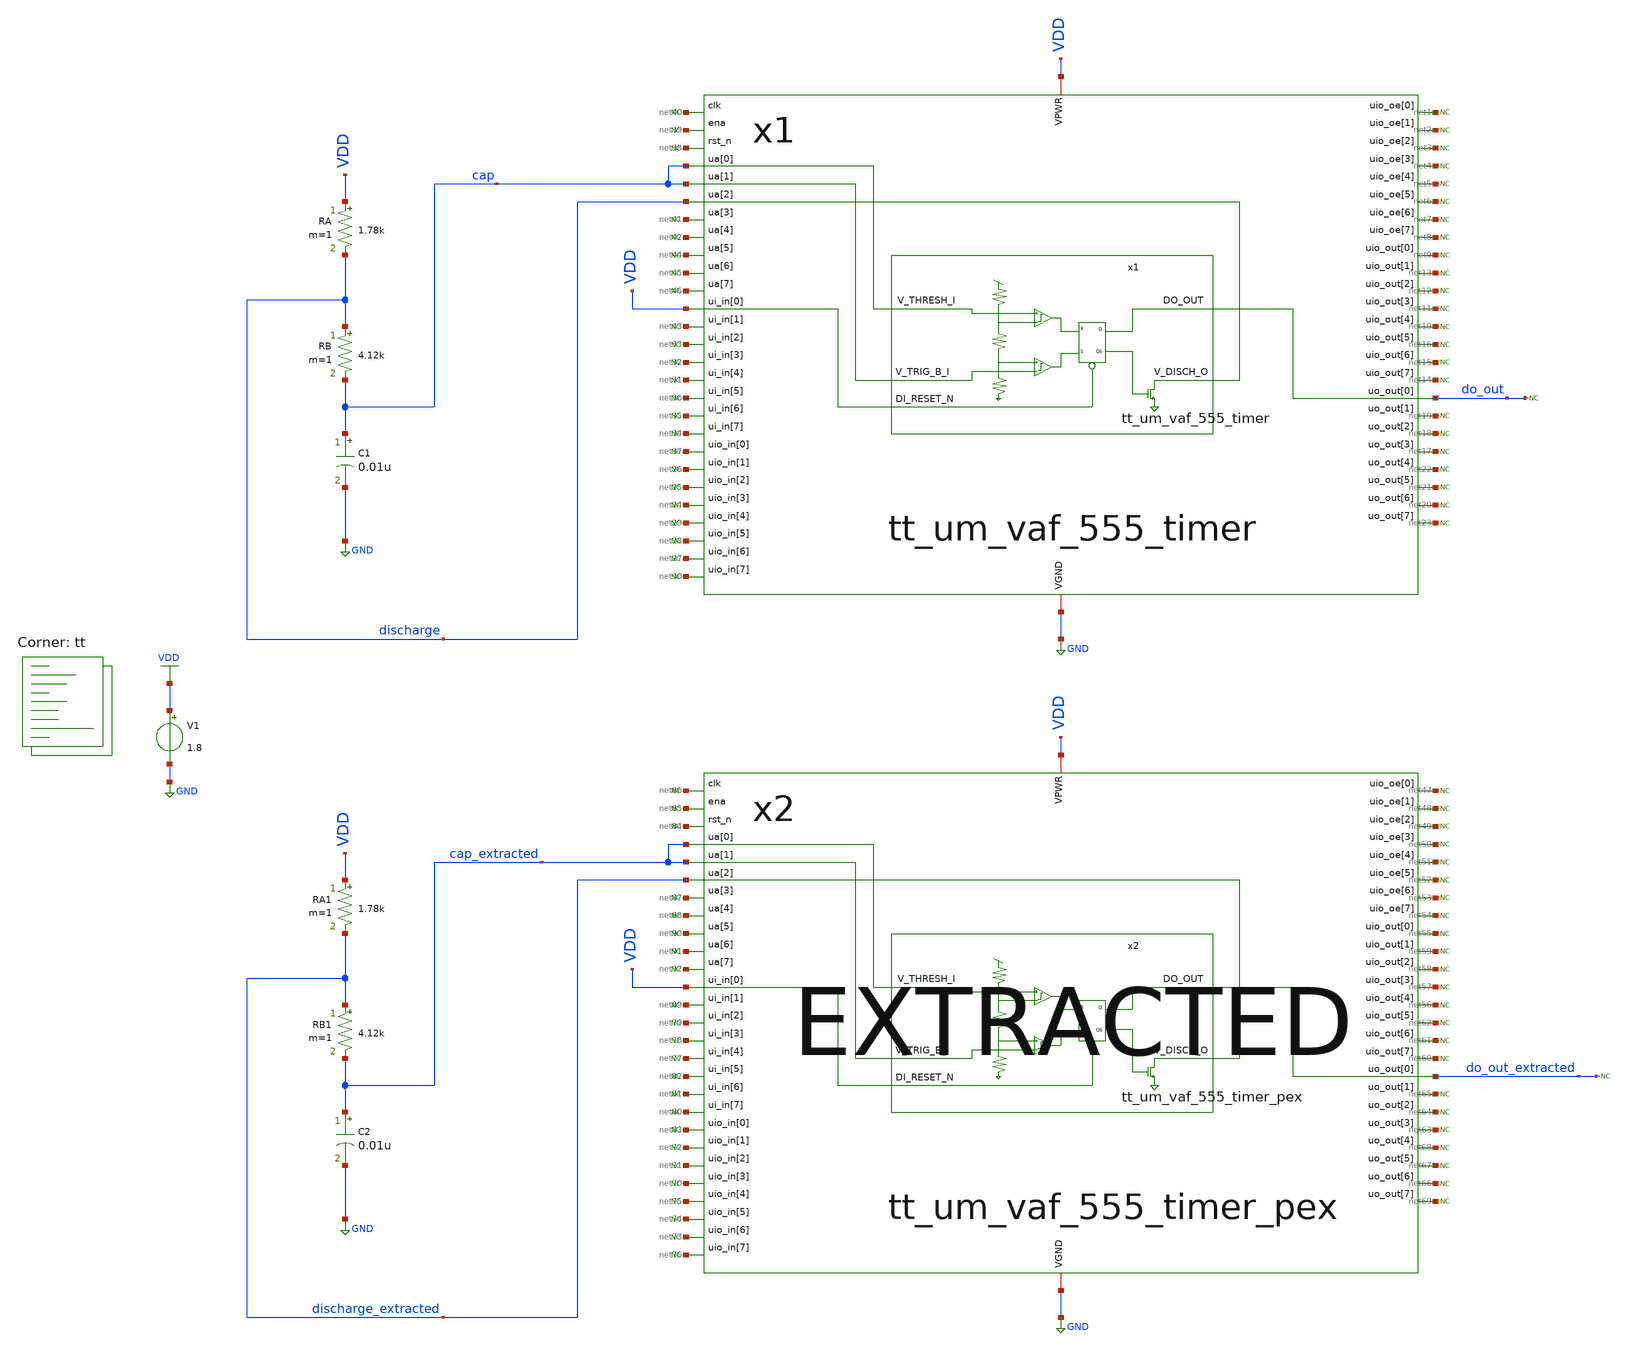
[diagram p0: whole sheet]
** sch_path: xsch/tb/tt_um_vaf_555_timer/tb_tt_um_vaf_555_timer_astable.sch
**.subckt tb_tt_um_vaf_555_timer_astable
V1 VDD GND 1.8
.save i(v1)
RA VDD discharge 1.78k m=1
RB discharge cap 4.12k m=1
C1 cap GND 0.01u m=1
* noconn do_out
* noconn #net1
* noconn #net2
* noconn #net3
* noconn #net4
* noconn #net5
* noconn #net6
* noconn #net7
* noconn #net8
* noconn #net9
* noconn #net10
* noconn #net11
* noconn #net12
* noconn #net13
* noconn #net14
* noconn #net15
* noconn #net16
* noconn #net17
* noconn #net18
* noconn #net19
* noconn #net20
* noconn #net21
* noconn #net22
* noconn #net23
* noconn #net24
* noconn #net25
* noconn #net26
* noconn #net27
* noconn #net28
* noconn #net29
* noconn #net30
* noconn #net31
* noconn #net32
* noconn #net33
* noconn #net34
* noconn #net35
* noconn #net36
* noconn #net37
* noconn #net38
* noconn #net39
* noconn #net40
* noconn #net41
* noconn #net42
* noconn #net43
x1 net40 net39 net38 cap cap discharge net41 net42 net44 net45 net46 VDD net43 net33 net32 net31
+ net36 net35 net34 net37 net26 net25 net24 net29 net28 net27 net30 net1 net2 net3 net4 net5 net6 net7 net8
+ net9 net13 net12 net11 net10 net16 net15 net14 do_out net19 net18 net17 net22 net21 net20 net23 VDD GND
+ tt_um_vaf_555_timer
* noconn #net44
* noconn #net45
* noconn #net46
RA1 VDD discharge_extracted 1.78k m=1
RB1 discharge_extracted cap_extracted 4.12k m=1
C2 cap_extracted GND 0.01u m=1
* noconn do_out_extracted
* noconn #net47
* noconn #net48
* noconn #net49
* noconn #net50
* noconn #net51
* noconn #net52
* noconn #net53
* noconn #net54
* noconn #net55
* noconn #net56
* noconn #net57
* noconn #net58
* noconn #net59
* noconn #net60
* noconn #net61
* noconn #net62
* noconn #net63
* noconn #net64
* noconn #net65
* noconn #net66
* noconn #net67
* noconn #net68
* noconn #net69
* noconn #net70
* noconn #net71
* noconn #net72
* noconn #net73
* noconn #net74
* noconn #net75
* noconn #net76
* noconn #net77
* noconn #net78
* noconn #net79
* noconn #net80
* noconn #net81
* noconn #net82
* noconn #net83
* noconn #net84
* noconn #net85
* noconn #net86
* noconn #net87
* noconn #net88
* noconn #net89
* noconn #net90
* noconn #net91
* noconn #net92
x2 net86 net85 net84 cap_extracted cap_extracted discharge_extracted net87 net88 net90 net91 net92
+ VDD net89 net79 net78 net77 net82 net81 net80 net83 net72 net71 net70 net75 net74 net73 net76 net47
+ net48 net49 net50 net51 net52 net53 net54 net55 net59 net58 net57 net56 net62 net61 net60
+ do_out_extracted net65 net64 net63 net68 net67 net66 net69 VDD GND tt_um_vaf_555_timer_pex
**** begin user architecture code



.ic v(cap) = 0
.ic v(cap_pex) = 0

.control
	tran 0.1u 400u

	meas tran thigh trig v(do_out) val=0.9 rise=3 targ v(do_out) val=0.9 fall=4
	meas tran tlow trig v(do_out) val=0.9 fall=4 targ v(do_out) val=0.9 rise=4

	meas tran thigh_ext trig v(do_out_extracted) val=0.9 rise=3 targ v(do_out_extracted) val=0.9 fall=4
	meas tran tlow_ext trig v(do_out_extracted) val=0.9 fall=4 targ v(do_out_extracted) val=0.9 rise=4

	let period_meas = $&thigh + $&tlow;
	let freq_meas = 1/period_meas;

	let period_meas_ext = $&thigh_ext + $&tlow_ext;
	let freq_meas_ext = 1/period_meas_ext;
	echo --------------------
	echo Output High Schematic [seconds]: $&thigh
	echo Output Low Schematic [seconds]: $&tlow
	echo Frequency Schematic [Hz]: $&freq_meas
	echo --------------------
	echo Output High Extracted [seconds]: $&thigh_ext
	echo Output Low Extracted [seconds]: $&tlow_ext
	echo Frequency Extracted [Hz]: $&freq_meas_ext
	echo --------------------

	plot v(cap) v(do_out) ylabel 'Schematic'
	plot v(cap_extracted) v(do_out_extracted) ylabel 'Extracted'

.endc
.end


.lib $::SKYWATER_MODELS/sky130.lib.spice tt


.save v(do_out) v(discharge) v(cap) v(cap_extracted) v(do_out_extracted) v(discharge_extracted)
=

.savecurrents




.include ~/projects/tt06_555/xsch/ip/top/tt_um_vaf_555_timer/tt_um_vaf_555_timer_pex.spice


**** end user architecture code
**.ends
.GLOBAL VDD
.GLOBAL GND
.end
